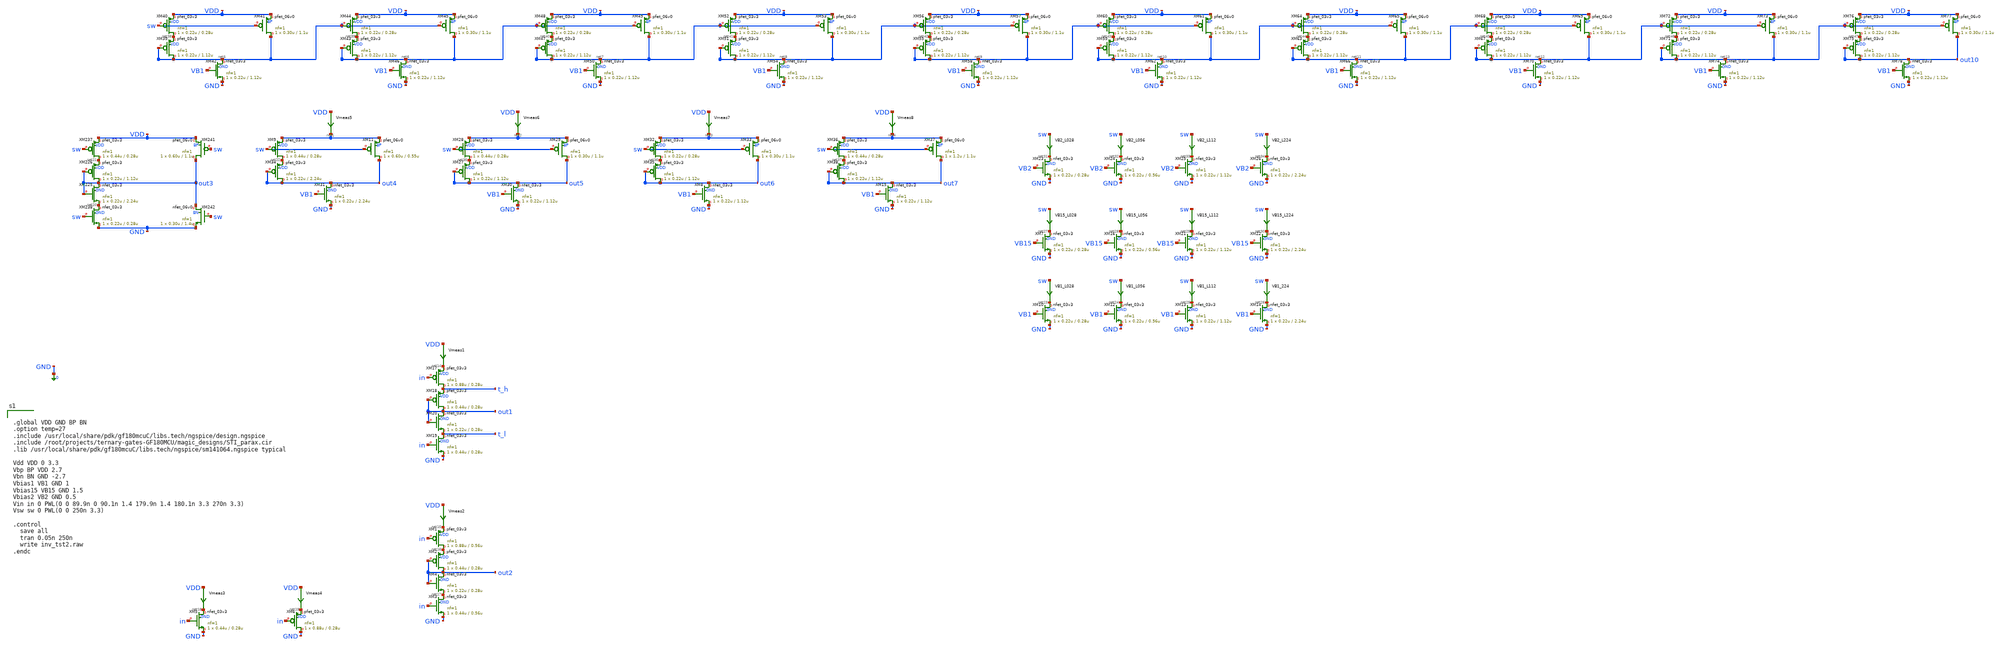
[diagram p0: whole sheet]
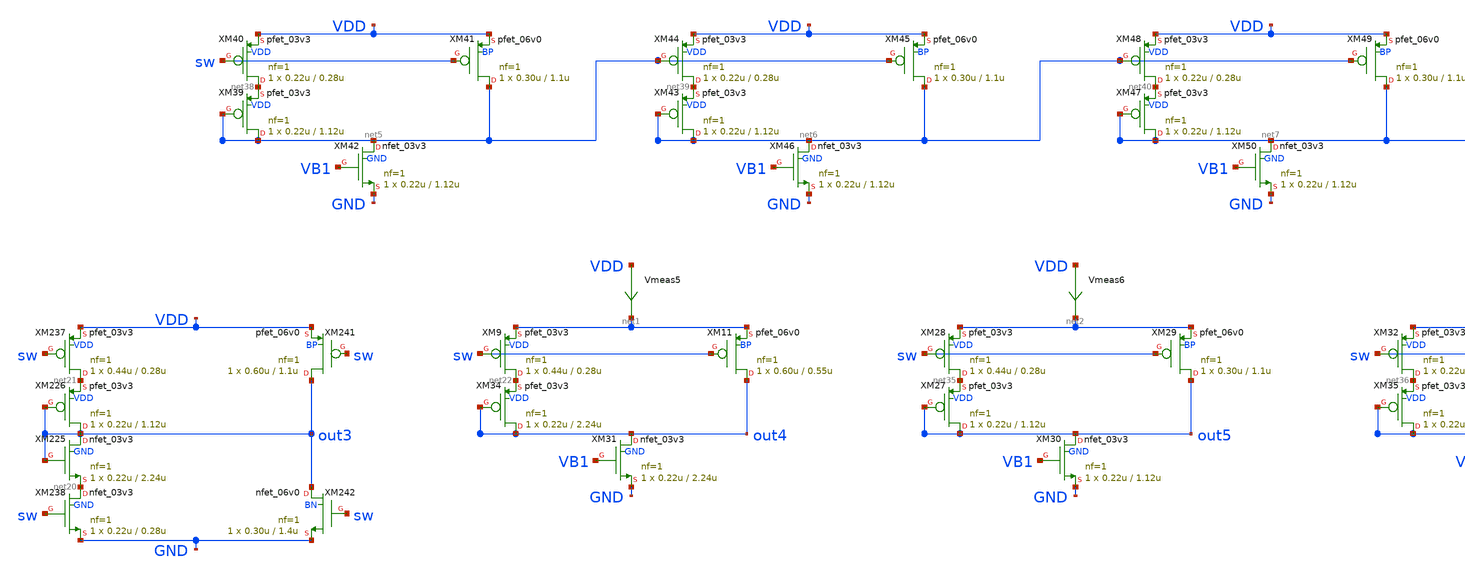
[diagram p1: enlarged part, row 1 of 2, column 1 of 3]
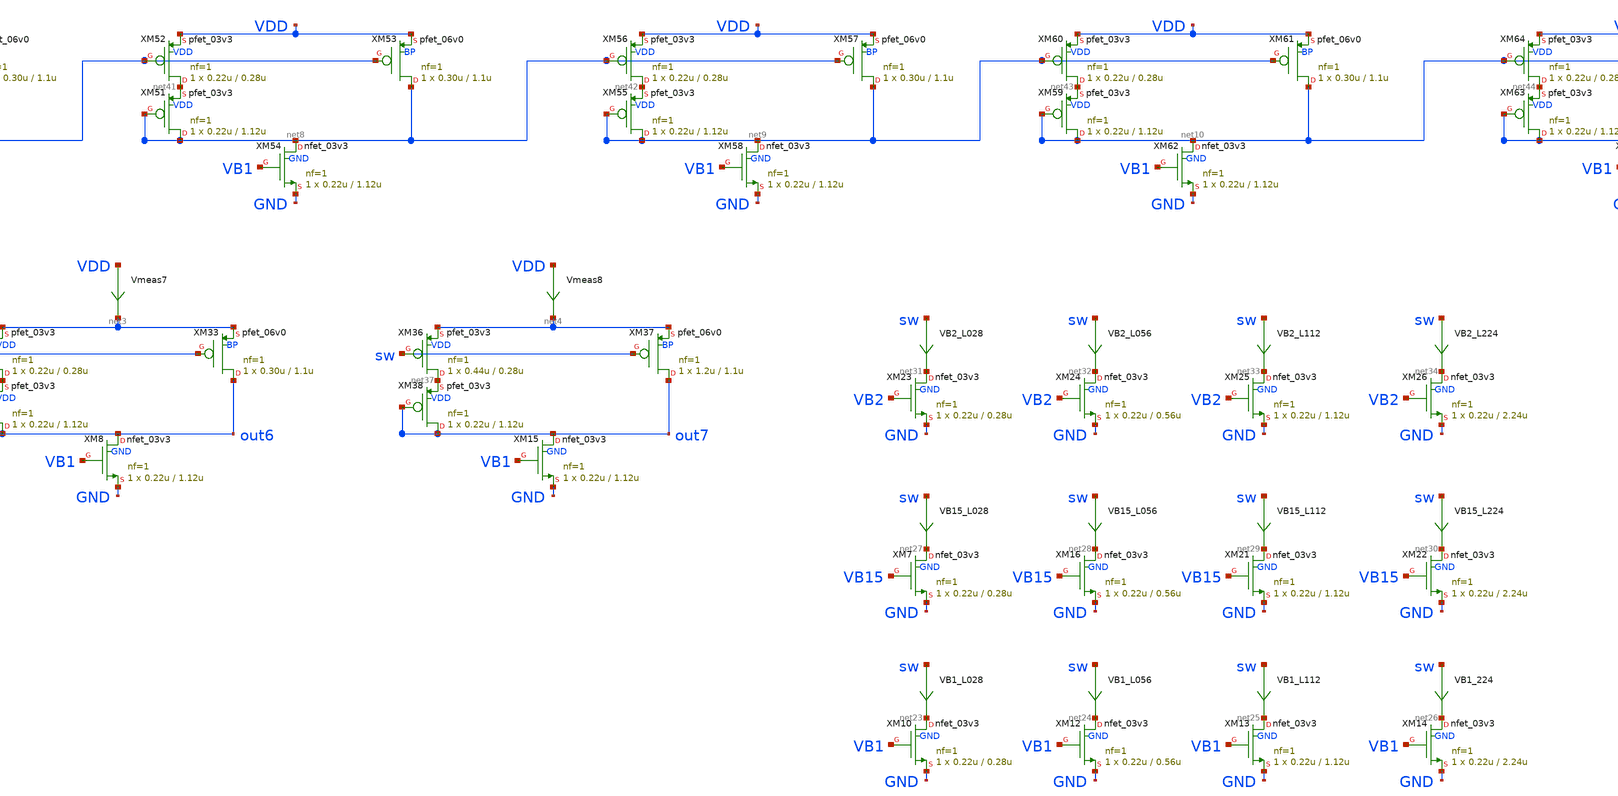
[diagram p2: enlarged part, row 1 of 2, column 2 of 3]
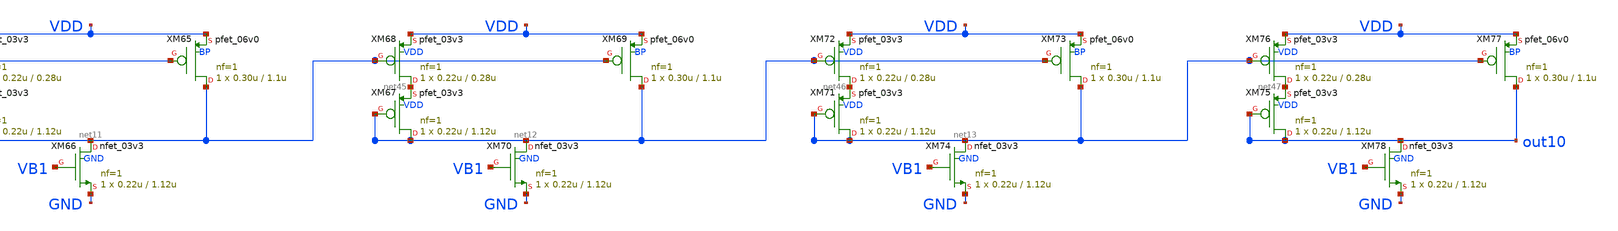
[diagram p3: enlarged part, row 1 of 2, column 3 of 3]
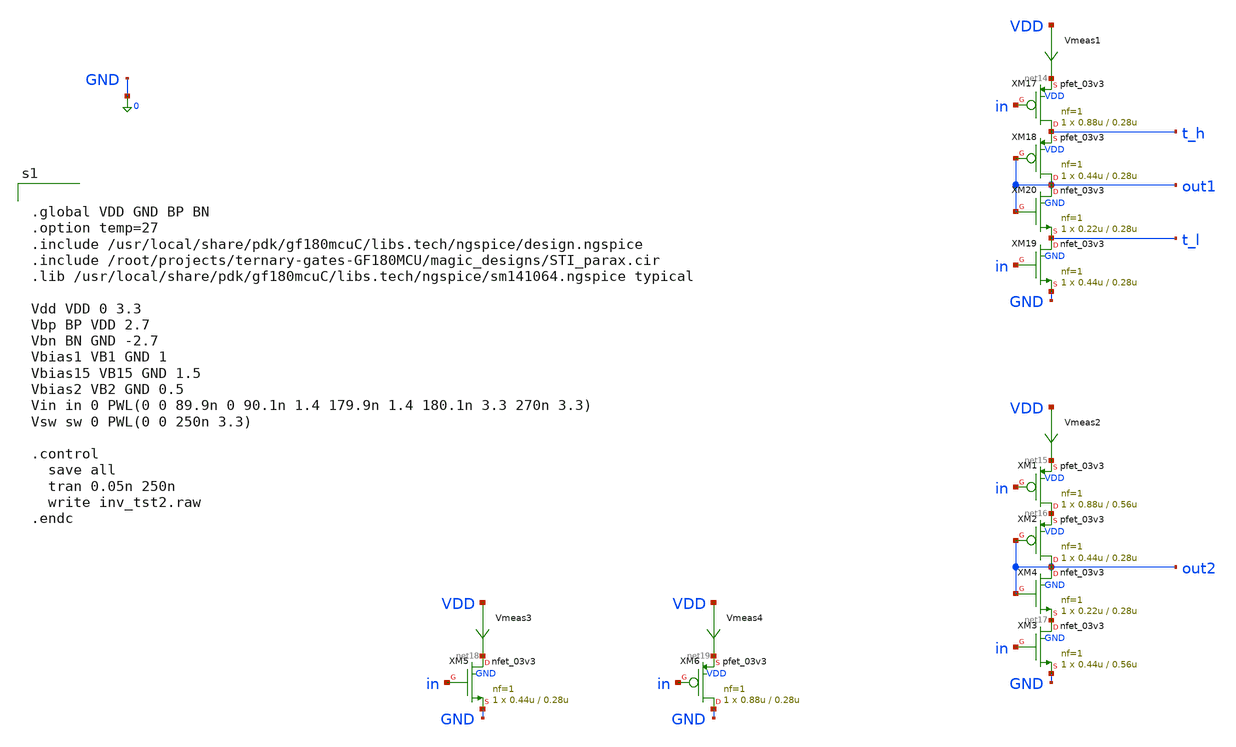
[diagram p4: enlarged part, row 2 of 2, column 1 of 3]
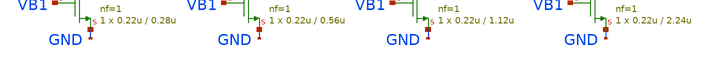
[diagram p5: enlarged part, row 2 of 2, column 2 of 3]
** sch_path: xschem_designs/inv_tst2.sch
**.subckt inv_tst2
Vmeas1 VDD net14 0
.save i(vmeas1)
XM17 t_h in net14 VDD pfet_03v3 L=0.28u W=0.88u nf=1 ad='int((nf+1)/2) * W/nf * 0.18u' as='int((nf+2)/2) * W/nf * 0.18u'
+ pd='2*int((nf+1)/2) * (W/nf + 0.18u)' ps='2*int((nf+2)/2) * (W/nf + 0.18u)' nrd='0.18u / W' nrs='0.18u / W'
+ sa=0 sb=0 sd=0 m=1 par=1
XM18 out1 out1 t_h VDD pfet_03v3 L=0.28u W=0.44u nf=1 ad='int((nf+1)/2) * W/nf * 0.18u' as='int((nf+2)/2) * W/nf * 0.18u'
+ pd='2*int((nf+1)/2) * (W/nf + 0.18u)' ps='2*int((nf+2)/2) * (W/nf + 0.18u)' nrd='0.18u / W' nrs='0.18u / W'
+ sa=0 sb=0 sd=0 m=1 par=1
XM19 t_l in GND GND nfet_03v3 L=0.28u W=0.44u nf=1 ad='int((nf+1)/2) * W/nf * 0.18u' as='int((nf+2)/2) * W/nf * 0.18u'
+ pd='2*int((nf+1)/2) * (W/nf + 0.18u)' ps='2*int((nf+2)/2) * (W/nf + 0.18u)' nrd='0.18u / W' nrs='0.18u / W'
+ sa=0 sb=0 sd=0 m=1 par=1
XM20 out1 out1 t_l GND nfet_03v3 L=0.28u W=0.22u nf=1 ad='int((nf+1)/2) * W/nf * 0.18u' as='int((nf+2)/2) * W/nf * 0.18u'
+ pd='2*int((nf+1)/2) * (W/nf + 0.18u)' ps='2*int((nf+2)/2) * (W/nf + 0.18u)' nrd='0.18u / W' nrs='0.18u / W'
+ sa=0 sb=0 sd=0 m=1 par=1
Vmeas2 VDD net15 0
.save i(vmeas2)
XM1 net16 in net15 VDD pfet_03v3 L=0.56u W=0.88u nf=1 ad='int((nf+1)/2) * W/nf * 0.18u' as='int((nf+2)/2) * W/nf * 0.18u'
+ pd='2*int((nf+1)/2) * (W/nf + 0.18u)' ps='2*int((nf+2)/2) * (W/nf + 0.18u)' nrd='0.18u / W' nrs='0.18u / W'
+ sa=0 sb=0 sd=0 m=1 par=1
XM2 out2 out2 net16 VDD pfet_03v3 L=0.28u W=0.44u nf=1 ad='int((nf+1)/2) * W/nf * 0.18u' as='int((nf+2)/2) * W/nf * 0.18u'
+ pd='2*int((nf+1)/2) * (W/nf + 0.18u)' ps='2*int((nf+2)/2) * (W/nf + 0.18u)' nrd='0.18u / W' nrs='0.18u / W'
+ sa=0 sb=0 sd=0 m=1 par=1
XM3 net17 in GND GND nfet_03v3 L=0.56u W=0.44u nf=1 ad='int((nf+1)/2) * W/nf * 0.18u' as='int((nf+2)/2) * W/nf * 0.18u'
+ pd='2*int((nf+1)/2) * (W/nf + 0.18u)' ps='2*int((nf+2)/2) * (W/nf + 0.18u)' nrd='0.18u / W' nrs='0.18u / W'
+ sa=0 sb=0 sd=0 m=1 par=1
XM4 out2 out2 net17 GND nfet_03v3 L=0.28u W=0.22u nf=1 ad='int((nf+1)/2) * W/nf * 0.18u' as='int((nf+2)/2) * W/nf * 0.18u'
+ pd='2*int((nf+1)/2) * (W/nf + 0.18u)' ps='2*int((nf+2)/2) * (W/nf + 0.18u)' nrd='0.18u / W' nrs='0.18u / W'
+ sa=0 sb=0 sd=0 m=1 par=1
XM5 net18 in GND GND nfet_03v3 L=0.28u W=0.44u nf=1 ad='int((nf+1)/2) * W/nf * 0.18u' as='int((nf+2)/2) * W/nf * 0.18u'
+ pd='2*int((nf+1)/2) * (W/nf + 0.18u)' ps='2*int((nf+2)/2) * (W/nf + 0.18u)' nrd='0.18u / W' nrs='0.18u / W'
+ sa=0 sb=0 sd=0 m=1 par=1
Vmeas3 VDD net18 0
.save i(vmeas3)
Vmeas4 VDD net19 0
.save i(vmeas4)
XM6 GND in net19 VDD pfet_03v3 L=0.28u W=0.88u nf=1 ad='int((nf+1)/2) * W/nf * 0.18u' as='int((nf+2)/2) * W/nf * 0.18u'
+ pd='2*int((nf+1)/2) * (W/nf + 0.18u)' ps='2*int((nf+2)/2) * (W/nf + 0.18u)' nrd='0.18u / W' nrs='0.18u / W'
+ sa=0 sb=0 sd=0 m=1 par=1
XM225 out3 out3 net20 GND nfet_03v3 L=2.24u W=0.22u nf=1 ad='int((nf+1)/2) * W/nf * 0.18u' as='int((nf+2)/2) * W/nf * 0.18u'
+ pd='2*int((nf+1)/2) * (W/nf + 0.18u)' ps='2*int((nf+2)/2) * (W/nf + 0.18u)' nrd='0.18u / W' nrs='0.18u / W'
+ sa=0 sb=0 sd=0 m=1 par=1
XM226 out3 out3 net21 VDD pfet_03v3 L=1.12u W=0.22u nf=1 ad='int((nf+1)/2) * W/nf * 0.18u' as='int((nf+2)/2) * W/nf * 0.18u'
+ pd='2*int((nf+1)/2) * (W/nf + 0.18u)' ps='2*int((nf+2)/2) * (W/nf + 0.18u)' nrd='0.18u / W' nrs='0.18u / W'
+ sa=0 sb=0 sd=0 m=1 par=1
XM237 net21 sw VDD VDD pfet_03v3 L=0.28u W=0.44u nf=1 ad='int((nf+1)/2) * W/nf * 0.18u' as='int((nf+2)/2) * W/nf * 0.18u'
+ pd='2*int((nf+1)/2) * (W/nf + 0.18u)' ps='2*int((nf+2)/2) * (W/nf + 0.18u)' nrd='0.18u / W' nrs='0.18u / W'
+ sa=0 sb=0 sd=0 m=1 par=1
XM238 net20 sw GND GND nfet_03v3 L=0.28u W=0.22u nf=1 ad='int((nf+1)/2) * W/nf * 0.18u' as='int((nf+2)/2) * W/nf * 0.18u'
+ pd='2*int((nf+1)/2) * (W/nf + 0.18u)' ps='2*int((nf+2)/2) * (W/nf + 0.18u)' nrd='0.18u / W' nrs='0.18u / W'
+ sa=0 sb=0 sd=0 m=1 par=1
XM241 out3 sw VDD BP pfet_06v0 L=1.1u W=0.60u nf=1 ad='int((nf+1)/2) * W/nf * 0.18u' as='int((nf+2)/2) * W/nf * 0.18u'
+ pd='2*int((nf+1)/2) * (W/nf + 0.18u)' ps='2*int((nf+2)/2) * (W/nf + 0.18u)' nrd='0.18u / W' nrs='0.18u / W'
+ sa=0 sb=0 sd=0 m=1 par=1
XM242 out3 sw GND BN nfet_06v0 L=1.4u W=0.30u nf=1 ad='int((nf+1)/2) * W/nf * 0.18u' as='int((nf+2)/2) * W/nf * 0.18u'
+ pd='2*int((nf+1)/2) * (W/nf + 0.18u)' ps='2*int((nf+2)/2) * (W/nf + 0.18u)' nrd='0.18u / W' nrs='0.18u / W'
+ sa=0 sb=0 sd=0 m=1 par=1
XM9 net22 sw net1 VDD pfet_03v3 L=0.28u W=0.44u nf=1 ad='int((nf+1)/2) * W/nf * 0.18u' as='int((nf+2)/2) * W/nf * 0.18u'
+ pd='2*int((nf+1)/2) * (W/nf + 0.18u)' ps='2*int((nf+2)/2) * (W/nf + 0.18u)' nrd='0.18u / W' nrs='0.18u / W'
+ sa=0 sb=0 sd=0 m=1 par=1
XM11 out4 sw net1 BP pfet_06v0 L=0.55u W=0.60u nf=1 ad='int((nf+1)/2) * W/nf * 0.18u' as='int((nf+2)/2) * W/nf * 0.18u'
+ pd='2*int((nf+1)/2) * (W/nf + 0.18u)' ps='2*int((nf+2)/2) * (W/nf + 0.18u)' nrd='0.18u / W' nrs='0.18u / W'
+ sa=0 sb=0 sd=0 m=1 par=1
Vmeas5 VDD net1 0
.save i(vmeas5)
XM10 net23 VB1 GND GND nfet_03v3 L=0.28u W=0.22u nf=1 ad='int((nf+1)/2) * W/nf * 0.18u' as='int((nf+2)/2) * W/nf * 0.18u'
+ pd='2*int((nf+1)/2) * (W/nf + 0.18u)' ps='2*int((nf+2)/2) * (W/nf + 0.18u)' nrd='0.18u / W' nrs='0.18u / W'
+ sa=0 sb=0 sd=0 m=1 par=1
VB1_L028 sw net23 0
.save i(vb1_l028)
XM12 net24 VB1 GND GND nfet_03v3 L=0.56u W=0.22u nf=1 ad='int((nf+1)/2) * W/nf * 0.18u' as='int((nf+2)/2) * W/nf * 0.18u'
+ pd='2*int((nf+1)/2) * (W/nf + 0.18u)' ps='2*int((nf+2)/2) * (W/nf + 0.18u)' nrd='0.18u / W' nrs='0.18u / W'
+ sa=0 sb=0 sd=0 m=1 par=1
XM13 net25 VB1 GND GND nfet_03v3 L=1.12u W=0.22u nf=1 ad='int((nf+1)/2) * W/nf * 0.18u' as='int((nf+2)/2) * W/nf * 0.18u'
+ pd='2*int((nf+1)/2) * (W/nf + 0.18u)' ps='2*int((nf+2)/2) * (W/nf + 0.18u)' nrd='0.18u / W' nrs='0.18u / W'
+ sa=0 sb=0 sd=0 m=1 par=1
XM14 net26 VB1 GND GND nfet_03v3 L=2.24u W=0.22u nf=1 ad='int((nf+1)/2) * W/nf * 0.18u' as='int((nf+2)/2) * W/nf * 0.18u'
+ pd='2*int((nf+1)/2) * (W/nf + 0.18u)' ps='2*int((nf+2)/2) * (W/nf + 0.18u)' nrd='0.18u / W' nrs='0.18u / W'
+ sa=0 sb=0 sd=0 m=1 par=1
VB1_L056 sw net24 0
.save i(vb1_l056)
VB1_L112 sw net25 0
.save i(vb1_l112)
VB1_224 sw net26 0
.save i(vb1_224)
XM7 net27 VB15 GND GND nfet_03v3 L=0.28u W=0.22u nf=1 ad='int((nf+1)/2) * W/nf * 0.18u' as='int((nf+2)/2) * W/nf * 0.18u'
+ pd='2*int((nf+1)/2) * (W/nf + 0.18u)' ps='2*int((nf+2)/2) * (W/nf + 0.18u)' nrd='0.18u / W' nrs='0.18u / W'
+ sa=0 sb=0 sd=0 m=1 par=1
VB15_L028 sw net27 0
.save i(vb15_l028)
XM16 net28 VB15 GND GND nfet_03v3 L=0.56u W=0.22u nf=1 ad='int((nf+1)/2) * W/nf * 0.18u' as='int((nf+2)/2) * W/nf * 0.18u'
+ pd='2*int((nf+1)/2) * (W/nf + 0.18u)' ps='2*int((nf+2)/2) * (W/nf + 0.18u)' nrd='0.18u / W' nrs='0.18u / W'
+ sa=0 sb=0 sd=0 m=1 par=1
XM21 net29 VB15 GND GND nfet_03v3 L=1.12u W=0.22u nf=1 ad='int((nf+1)/2) * W/nf * 0.18u' as='int((nf+2)/2) * W/nf * 0.18u'
+ pd='2*int((nf+1)/2) * (W/nf + 0.18u)' ps='2*int((nf+2)/2) * (W/nf + 0.18u)' nrd='0.18u / W' nrs='0.18u / W'
+ sa=0 sb=0 sd=0 m=1 par=1
XM22 net30 VB15 GND GND nfet_03v3 L=2.24u W=0.22u nf=1 ad='int((nf+1)/2) * W/nf * 0.18u' as='int((nf+2)/2) * W/nf * 0.18u'
+ pd='2*int((nf+1)/2) * (W/nf + 0.18u)' ps='2*int((nf+2)/2) * (W/nf + 0.18u)' nrd='0.18u / W' nrs='0.18u / W'
+ sa=0 sb=0 sd=0 m=1 par=1
VB15_L056 sw net28 0
.save i(vb15_l056)
VB15_L112 sw net29 0
.save i(vb15_l112)
VB15_L224 sw net30 0
.save i(vb15_l224)
XM23 net31 VB2 GND GND nfet_03v3 L=0.28u W=0.22u nf=1 ad='int((nf+1)/2) * W/nf * 0.18u' as='int((nf+2)/2) * W/nf * 0.18u'
+ pd='2*int((nf+1)/2) * (W/nf + 0.18u)' ps='2*int((nf+2)/2) * (W/nf + 0.18u)' nrd='0.18u / W' nrs='0.18u / W'
+ sa=0 sb=0 sd=0 m=1 par=1
VB2_L028 sw net31 0
.save i(vb2_l028)
XM24 net32 VB2 GND GND nfet_03v3 L=0.56u W=0.22u nf=1 ad='int((nf+1)/2) * W/nf * 0.18u' as='int((nf+2)/2) * W/nf * 0.18u'
+ pd='2*int((nf+1)/2) * (W/nf + 0.18u)' ps='2*int((nf+2)/2) * (W/nf + 0.18u)' nrd='0.18u / W' nrs='0.18u / W'
+ sa=0 sb=0 sd=0 m=1 par=1
XM25 net33 VB2 GND GND nfet_03v3 L=1.12u W=0.22u nf=1 ad='int((nf+1)/2) * W/nf * 0.18u' as='int((nf+2)/2) * W/nf * 0.18u'
+ pd='2*int((nf+1)/2) * (W/nf + 0.18u)' ps='2*int((nf+2)/2) * (W/nf + 0.18u)' nrd='0.18u / W' nrs='0.18u / W'
+ sa=0 sb=0 sd=0 m=1 par=1
XM26 net34 VB2 GND GND nfet_03v3 L=2.24u W=0.22u nf=1 ad='int((nf+1)/2) * W/nf * 0.18u' as='int((nf+2)/2) * W/nf * 0.18u'
+ pd='2*int((nf+1)/2) * (W/nf + 0.18u)' ps='2*int((nf+2)/2) * (W/nf + 0.18u)' nrd='0.18u / W' nrs='0.18u / W'
+ sa=0 sb=0 sd=0 m=1 par=1
VB2_L056 sw net32 0
.save i(vb2_l056)
VB2_L112 sw net33 0
.save i(vb2_l112)
VB2_L224 sw net34 0
.save i(vb2_l224)
XM28 net35 sw net2 VDD pfet_03v3 L=0.28u W=0.44u nf=1 ad='int((nf+1)/2) * W/nf * 0.18u' as='int((nf+2)/2) * W/nf * 0.18u'
+ pd='2*int((nf+1)/2) * (W/nf + 0.18u)' ps='2*int((nf+2)/2) * (W/nf + 0.18u)' nrd='0.18u / W' nrs='0.18u / W'
+ sa=0 sb=0 sd=0 m=1 par=1
XM29 out5 sw net2 BP pfet_06v0 L=1.1u W=0.30u nf=1 ad='int((nf+1)/2) * W/nf * 0.18u' as='int((nf+2)/2) * W/nf * 0.18u'
+ pd='2*int((nf+1)/2) * (W/nf + 0.18u)' ps='2*int((nf+2)/2) * (W/nf + 0.18u)' nrd='0.18u / W' nrs='0.18u / W'
+ sa=0 sb=0 sd=0 m=1 par=1
Vmeas6 VDD net2 0
.save i(vmeas6)
XM32 net36 sw net3 VDD pfet_03v3 L=0.28u W=0.22u nf=1 ad='int((nf+1)/2) * W/nf * 0.18u' as='int((nf+2)/2) * W/nf * 0.18u'
+ pd='2*int((nf+1)/2) * (W/nf + 0.18u)' ps='2*int((nf+2)/2) * (W/nf + 0.18u)' nrd='0.18u / W' nrs='0.18u / W'
+ sa=0 sb=0 sd=0 m=1 par=1
Vmeas7 VDD net3 0
.save i(vmeas7)
XM36 net37 sw net4 VDD pfet_03v3 L=0.28u W=0.44u nf=1 ad='int((nf+1)/2) * W/nf * 0.18u' as='int((nf+2)/2) * W/nf * 0.18u'
+ pd='2*int((nf+1)/2) * (W/nf + 0.18u)' ps='2*int((nf+2)/2) * (W/nf + 0.18u)' nrd='0.18u / W' nrs='0.18u / W'
+ sa=0 sb=0 sd=0 m=1 par=1
XM37 out7 sw net4 BP pfet_06v0 L=1.1u W=1.2u nf=1 ad='int((nf+1)/2) * W/nf * 0.18u' as='int((nf+2)/2) * W/nf * 0.18u'
+ pd='2*int((nf+1)/2) * (W/nf + 0.18u)' ps='2*int((nf+2)/2) * (W/nf + 0.18u)' nrd='0.18u / W' nrs='0.18u / W'
+ sa=0 sb=0 sd=0 m=1 par=1
Vmeas8 VDD net4 0
.save i(vmeas8)
XM8 out6 VB1 GND GND nfet_03v3 L=1.12u W=0.22u nf=1 ad='int((nf+1)/2) * W/nf * 0.18u' as='int((nf+2)/2) * W/nf * 0.18u'
+ pd='2*int((nf+1)/2) * (W/nf + 0.18u)' ps='2*int((nf+2)/2) * (W/nf + 0.18u)' nrd='0.18u / W' nrs='0.18u / W'
+ sa=0 sb=0 sd=0 m=1 par=1
XM15 out7 VB1 GND GND nfet_03v3 L=1.12u W=0.22u nf=1 ad='int((nf+1)/2) * W/nf * 0.18u' as='int((nf+2)/2) * W/nf * 0.18u'
+ pd='2*int((nf+1)/2) * (W/nf + 0.18u)' ps='2*int((nf+2)/2) * (W/nf + 0.18u)' nrd='0.18u / W' nrs='0.18u / W'
+ sa=0 sb=0 sd=0 m=1 par=1
XM31 out4 VB1 GND GND nfet_03v3 L=2.24u W=0.22u nf=1 ad='int((nf+1)/2) * W/nf * 0.18u' as='int((nf+2)/2) * W/nf * 0.18u'
+ pd='2*int((nf+1)/2) * (W/nf + 0.18u)' ps='2*int((nf+2)/2) * (W/nf + 0.18u)' nrd='0.18u / W' nrs='0.18u / W'
+ sa=0 sb=0 sd=0 m=1 par=1
XM34 out4 out4 net22 VDD pfet_03v3 L=2.24u W=0.22u nf=1 ad='int((nf+1)/2) * W/nf * 0.18u' as='int((nf+2)/2) * W/nf * 0.18u'
+ pd='2*int((nf+1)/2) * (W/nf + 0.18u)' ps='2*int((nf+2)/2) * (W/nf + 0.18u)' nrd='0.18u / W' nrs='0.18u / W'
+ sa=0 sb=0 sd=0 m=1 par=1
XM35 out6 out6 net36 VDD pfet_03v3 L=1.12u W=0.22u nf=1 ad='int((nf+1)/2) * W/nf * 0.18u' as='int((nf+2)/2) * W/nf * 0.18u'
+ pd='2*int((nf+1)/2) * (W/nf + 0.18u)' ps='2*int((nf+2)/2) * (W/nf + 0.18u)' nrd='0.18u / W' nrs='0.18u / W'
+ sa=0 sb=0 sd=0 m=1 par=1
XM38 out7 out7 net37 VDD pfet_03v3 L=1.12u W=0.22u nf=1 ad='int((nf+1)/2) * W/nf * 0.18u' as='int((nf+2)/2) * W/nf * 0.18u'
+ pd='2*int((nf+1)/2) * (W/nf + 0.18u)' ps='2*int((nf+2)/2) * (W/nf + 0.18u)' nrd='0.18u / W' nrs='0.18u / W'
+ sa=0 sb=0 sd=0 m=1 par=1
XM39 net5 net5 net38 VDD pfet_03v3 L=1.12u W=0.22u nf=1 ad='int((nf+1)/2) * W/nf * 0.18u' as='int((nf+2)/2) * W/nf * 0.18u'
+ pd='2*int((nf+1)/2) * (W/nf + 0.18u)' ps='2*int((nf+2)/2) * (W/nf + 0.18u)' nrd='0.18u / W' nrs='0.18u / W'
+ sa=0 sb=0 sd=0 m=1 par=1
XM42 net5 VB1 GND GND nfet_03v3 L=1.12u W=0.22u nf=1 ad='int((nf+1)/2) * W/nf * 0.18u' as='int((nf+2)/2) * W/nf * 0.18u'
+ pd='2*int((nf+1)/2) * (W/nf + 0.18u)' ps='2*int((nf+2)/2) * (W/nf + 0.18u)' nrd='0.18u / W' nrs='0.18u / W'
+ sa=0 sb=0 sd=0 m=1 par=1
XM43 net6 net6 net39 VDD pfet_03v3 L=1.12u W=0.22u nf=1 ad='int((nf+1)/2) * W/nf * 0.18u' as='int((nf+2)/2) * W/nf * 0.18u'
+ pd='2*int((nf+1)/2) * (W/nf + 0.18u)' ps='2*int((nf+2)/2) * (W/nf + 0.18u)' nrd='0.18u / W' nrs='0.18u / W'
+ sa=0 sb=0 sd=0 m=1 par=1
XM46 net6 VB1 GND GND nfet_03v3 L=1.12u W=0.22u nf=1 ad='int((nf+1)/2) * W/nf * 0.18u' as='int((nf+2)/2) * W/nf * 0.18u'
+ pd='2*int((nf+1)/2) * (W/nf + 0.18u)' ps='2*int((nf+2)/2) * (W/nf + 0.18u)' nrd='0.18u / W' nrs='0.18u / W'
+ sa=0 sb=0 sd=0 m=1 par=1
XM47 net7 net7 net40 VDD pfet_03v3 L=1.12u W=0.22u nf=1 ad='int((nf+1)/2) * W/nf * 0.18u' as='int((nf+2)/2) * W/nf * 0.18u'
+ pd='2*int((nf+1)/2) * (W/nf + 0.18u)' ps='2*int((nf+2)/2) * (W/nf + 0.18u)' nrd='0.18u / W' nrs='0.18u / W'
+ sa=0 sb=0 sd=0 m=1 par=1
XM50 net7 VB1 GND GND nfet_03v3 L=1.12u W=0.22u nf=1 ad='int((nf+1)/2) * W/nf * 0.18u' as='int((nf+2)/2) * W/nf * 0.18u'
+ pd='2*int((nf+1)/2) * (W/nf + 0.18u)' ps='2*int((nf+2)/2) * (W/nf + 0.18u)' nrd='0.18u / W' nrs='0.18u / W'
+ sa=0 sb=0 sd=0 m=1 par=1
XM51 net8 net8 net41 VDD pfet_03v3 L=1.12u W=0.22u nf=1 ad='int((nf+1)/2) * W/nf * 0.18u' as='int((nf+2)/2) * W/nf * 0.18u'
+ pd='2*int((nf+1)/2) * (W/nf + 0.18u)' ps='2*int((nf+2)/2) * (W/nf + 0.18u)' nrd='0.18u / W' nrs='0.18u / W'
+ sa=0 sb=0 sd=0 m=1 par=1
XM54 net8 VB1 GND GND nfet_03v3 L=1.12u W=0.22u nf=1 ad='int((nf+1)/2) * W/nf * 0.18u' as='int((nf+2)/2) * W/nf * 0.18u'
+ pd='2*int((nf+1)/2) * (W/nf + 0.18u)' ps='2*int((nf+2)/2) * (W/nf + 0.18u)' nrd='0.18u / W' nrs='0.18u / W'
+ sa=0 sb=0 sd=0 m=1 par=1
XM55 net9 net9 net42 VDD pfet_03v3 L=1.12u W=0.22u nf=1 ad='int((nf+1)/2) * W/nf * 0.18u' as='int((nf+2)/2) * W/nf * 0.18u'
+ pd='2*int((nf+1)/2) * (W/nf + 0.18u)' ps='2*int((nf+2)/2) * (W/nf + 0.18u)' nrd='0.18u / W' nrs='0.18u / W'
+ sa=0 sb=0 sd=0 m=1 par=1
XM58 net9 VB1 GND GND nfet_03v3 L=1.12u W=0.22u nf=1 ad='int((nf+1)/2) * W/nf * 0.18u' as='int((nf+2)/2) * W/nf * 0.18u'
+ pd='2*int((nf+1)/2) * (W/nf + 0.18u)' ps='2*int((nf+2)/2) * (W/nf + 0.18u)' nrd='0.18u / W' nrs='0.18u / W'
+ sa=0 sb=0 sd=0 m=1 par=1
XM59 net10 net10 net43 VDD pfet_03v3 L=1.12u W=0.22u nf=1 ad='int((nf+1)/2) * W/nf * 0.18u' as='int((nf+2)/2) * W/nf * 0.18u'
+ pd='2*int((nf+1)/2) * (W/nf + 0.18u)' ps='2*int((nf+2)/2) * (W/nf + 0.18u)' nrd='0.18u / W' nrs='0.18u / W'
+ sa=0 sb=0 sd=0 m=1 par=1
XM62 net10 VB1 GND GND nfet_03v3 L=1.12u W=0.22u nf=1 ad='int((nf+1)/2) * W/nf * 0.18u' as='int((nf+2)/2) * W/nf * 0.18u'
+ pd='2*int((nf+1)/2) * (W/nf + 0.18u)' ps='2*int((nf+2)/2) * (W/nf + 0.18u)' nrd='0.18u / W' nrs='0.18u / W'
+ sa=0 sb=0 sd=0 m=1 par=1
XM63 net11 net11 net44 VDD pfet_03v3 L=1.12u W=0.22u nf=1 ad='int((nf+1)/2) * W/nf * 0.18u' as='int((nf+2)/2) * W/nf * 0.18u'
+ pd='2*int((nf+1)/2) * (W/nf + 0.18u)' ps='2*int((nf+2)/2) * (W/nf + 0.18u)' nrd='0.18u / W' nrs='0.18u / W'
+ sa=0 sb=0 sd=0 m=1 par=1
XM66 net11 VB1 GND GND nfet_03v3 L=1.12u W=0.22u nf=1 ad='int((nf+1)/2) * W/nf * 0.18u' as='int((nf+2)/2) * W/nf * 0.18u'
+ pd='2*int((nf+1)/2) * (W/nf + 0.18u)' ps='2*int((nf+2)/2) * (W/nf + 0.18u)' nrd='0.18u / W' nrs='0.18u / W'
+ sa=0 sb=0 sd=0 m=1 par=1
XM67 net12 net12 net45 VDD pfet_03v3 L=1.12u W=0.22u nf=1 ad='int((nf+1)/2) * W/nf * 0.18u' as='int((nf+2)/2) * W/nf * 0.18u'
+ pd='2*int((nf+1)/2) * (W/nf + 0.18u)' ps='2*int((nf+2)/2) * (W/nf + 0.18u)' nrd='0.18u / W' nrs='0.18u / W'
+ sa=0 sb=0 sd=0 m=1 par=1
XM70 net12 VB1 GND GND nfet_03v3 L=1.12u W=0.22u nf=1 ad='int((nf+1)/2) * W/nf * 0.18u' as='int((nf+2)/2) * W/nf * 0.18u'
+ pd='2*int((nf+1)/2) * (W/nf + 0.18u)' ps='2*int((nf+2)/2) * (W/nf + 0.18u)' nrd='0.18u / W' nrs='0.18u / W'
+ sa=0 sb=0 sd=0 m=1 par=1
XM71 net13 net13 net46 VDD pfet_03v3 L=1.12u W=0.22u nf=1 ad='int((nf+1)/2) * W/nf * 0.18u' as='int((nf+2)/2) * W/nf * 0.18u'
+ pd='2*int((nf+1)/2) * (W/nf + 0.18u)' ps='2*int((nf+2)/2) * (W/nf + 0.18u)' nrd='0.18u / W' nrs='0.18u / W'
+ sa=0 sb=0 sd=0 m=1 par=1
XM74 net13 VB1 GND GND nfet_03v3 L=1.12u W=0.22u nf=1 ad='int((nf+1)/2) * W/nf * 0.18u' as='int((nf+2)/2) * W/nf * 0.18u'
+ pd='2*int((nf+1)/2) * (W/nf + 0.18u)' ps='2*int((nf+2)/2) * (W/nf + 0.18u)' nrd='0.18u / W' nrs='0.18u / W'
+ sa=0 sb=0 sd=0 m=1 par=1
XM75 out10 out10 net47 VDD pfet_03v3 L=1.12u W=0.22u nf=1 ad='int((nf+1)/2) * W/nf * 0.18u' as='int((nf+2)/2) * W/nf * 0.18u'
+ pd='2*int((nf+1)/2) * (W/nf + 0.18u)' ps='2*int((nf+2)/2) * (W/nf + 0.18u)' nrd='0.18u / W' nrs='0.18u / W'
+ sa=0 sb=0 sd=0 m=1 par=1
XM78 out10 VB1 GND GND nfet_03v3 L=1.12u W=0.22u nf=1 ad='int((nf+1)/2) * W/nf * 0.18u' as='int((nf+2)/2) * W/nf * 0.18u'
+ pd='2*int((nf+1)/2) * (W/nf + 0.18u)' ps='2*int((nf+2)/2) * (W/nf + 0.18u)' nrd='0.18u / W' nrs='0.18u / W'
+ sa=0 sb=0 sd=0 m=1 par=1
XM27 out5 out5 net35 VDD pfet_03v3 L=1.12u W=0.22u nf=1 ad='int((nf+1)/2) * W/nf * 0.18u' as='int((nf+2)/2) * W/nf * 0.18u'
+ pd='2*int((nf+1)/2) * (W/nf + 0.18u)' ps='2*int((nf+2)/2) * (W/nf + 0.18u)' nrd='0.18u / W' nrs='0.18u / W'
+ sa=0 sb=0 sd=0 m=1 par=1
XM30 out5 VB1 GND GND nfet_03v3 L=1.12u W=0.22u nf=1 ad='int((nf+1)/2) * W/nf * 0.18u' as='int((nf+2)/2) * W/nf * 0.18u'
+ pd='2*int((nf+1)/2) * (W/nf + 0.18u)' ps='2*int((nf+2)/2) * (W/nf + 0.18u)' nrd='0.18u / W' nrs='0.18u / W'
+ sa=0 sb=0 sd=0 m=1 par=1
XM41 net5 sw VDD BP pfet_06v0 L=1.1u W=0.30u nf=1 ad='int((nf+1)/2) * W/nf * 0.18u' as='int((nf+2)/2) * W/nf * 0.18u'
+ pd='2*int((nf+1)/2) * (W/nf + 0.18u)' ps='2*int((nf+2)/2) * (W/nf + 0.18u)' nrd='0.18u / W' nrs='0.18u / W'
+ sa=0 sb=0 sd=0 m=1 par=1
XM45 net6 net5 VDD BP pfet_06v0 L=1.1u W=0.30u nf=1 ad='int((nf+1)/2) * W/nf * 0.18u' as='int((nf+2)/2) * W/nf * 0.18u'
+ pd='2*int((nf+1)/2) * (W/nf + 0.18u)' ps='2*int((nf+2)/2) * (W/nf + 0.18u)' nrd='0.18u / W' nrs='0.18u / W'
+ sa=0 sb=0 sd=0 m=1 par=1
XM49 net7 net6 VDD BP pfet_06v0 L=1.1u W=0.30u nf=1 ad='int((nf+1)/2) * W/nf * 0.18u' as='int((nf+2)/2) * W/nf * 0.18u'
+ pd='2*int((nf+1)/2) * (W/nf + 0.18u)' ps='2*int((nf+2)/2) * (W/nf + 0.18u)' nrd='0.18u / W' nrs='0.18u / W'
+ sa=0 sb=0 sd=0 m=1 par=1
XM53 net8 net7 VDD BP pfet_06v0 L=1.1u W=0.30u nf=1 ad='int((nf+1)/2) * W/nf * 0.18u' as='int((nf+2)/2) * W/nf * 0.18u'
+ pd='2*int((nf+1)/2) * (W/nf + 0.18u)' ps='2*int((nf+2)/2) * (W/nf + 0.18u)' nrd='0.18u / W' nrs='0.18u / W'
+ sa=0 sb=0 sd=0 m=1 par=1
XM57 net9 net8 VDD BP pfet_06v0 L=1.1u W=0.30u nf=1 ad='int((nf+1)/2) * W/nf * 0.18u' as='int((nf+2)/2) * W/nf * 0.18u'
+ pd='2*int((nf+1)/2) * (W/nf + 0.18u)' ps='2*int((nf+2)/2) * (W/nf + 0.18u)' nrd='0.18u / W' nrs='0.18u / W'
+ sa=0 sb=0 sd=0 m=1 par=1
XM61 net10 net9 VDD BP pfet_06v0 L=1.1u W=0.30u nf=1 ad='int((nf+1)/2) * W/nf * 0.18u' as='int((nf+2)/2) * W/nf * 0.18u'
+ pd='2*int((nf+1)/2) * (W/nf + 0.18u)' ps='2*int((nf+2)/2) * (W/nf + 0.18u)' nrd='0.18u / W' nrs='0.18u / W'
+ sa=0 sb=0 sd=0 m=1 par=1
XM65 net11 net10 VDD BP pfet_06v0 L=1.1u W=0.30u nf=1 ad='int((nf+1)/2) * W/nf * 0.18u' as='int((nf+2)/2) * W/nf * 0.18u'
+ pd='2*int((nf+1)/2) * (W/nf + 0.18u)' ps='2*int((nf+2)/2) * (W/nf + 0.18u)' nrd='0.18u / W' nrs='0.18u / W'
+ sa=0 sb=0 sd=0 m=1 par=1
XM69 net12 net11 VDD BP pfet_06v0 L=1.1u W=0.30u nf=1 ad='int((nf+1)/2) * W/nf * 0.18u' as='int((nf+2)/2) * W/nf * 0.18u'
+ pd='2*int((nf+1)/2) * (W/nf + 0.18u)' ps='2*int((nf+2)/2) * (W/nf + 0.18u)' nrd='0.18u / W' nrs='0.18u / W'
+ sa=0 sb=0 sd=0 m=1 par=1
XM73 net13 net12 VDD BP pfet_06v0 L=1.1u W=0.30u nf=1 ad='int((nf+1)/2) * W/nf * 0.18u' as='int((nf+2)/2) * W/nf * 0.18u'
+ pd='2*int((nf+1)/2) * (W/nf + 0.18u)' ps='2*int((nf+2)/2) * (W/nf + 0.18u)' nrd='0.18u / W' nrs='0.18u / W'
+ sa=0 sb=0 sd=0 m=1 par=1
XM77 out10 net13 VDD BP pfet_06v0 L=1.1u W=0.30u nf=1 ad='int((nf+1)/2) * W/nf * 0.18u' as='int((nf+2)/2) * W/nf * 0.18u'
+ pd='2*int((nf+1)/2) * (W/nf + 0.18u)' ps='2*int((nf+2)/2) * (W/nf + 0.18u)' nrd='0.18u / W' nrs='0.18u / W'
+ sa=0 sb=0 sd=0 m=1 par=1
XM33 out6 sw net3 BP pfet_06v0 L=1.1u W=0.30u nf=1 ad='int((nf+1)/2) * W/nf * 0.18u' as='int((nf+2)/2) * W/nf * 0.18u'
+ pd='2*int((nf+1)/2) * (W/nf + 0.18u)' ps='2*int((nf+2)/2) * (W/nf + 0.18u)' nrd='0.18u / W' nrs='0.18u / W'
+ sa=0 sb=0 sd=0 m=1 par=1
XM40 net38 sw VDD VDD pfet_03v3 L=0.28u W=0.22u nf=1 ad='int((nf+1)/2) * W/nf * 0.18u' as='int((nf+2)/2) * W/nf * 0.18u'
+ pd='2*int((nf+1)/2) * (W/nf + 0.18u)' ps='2*int((nf+2)/2) * (W/nf + 0.18u)' nrd='0.18u / W' nrs='0.18u / W'
+ sa=0 sb=0 sd=0 m=1 par=1
XM44 net39 net5 VDD VDD pfet_03v3 L=0.28u W=0.22u nf=1 ad='int((nf+1)/2) * W/nf * 0.18u' as='int((nf+2)/2) * W/nf * 0.18u'
+ pd='2*int((nf+1)/2) * (W/nf + 0.18u)' ps='2*int((nf+2)/2) * (W/nf + 0.18u)' nrd='0.18u / W' nrs='0.18u / W'
+ sa=0 sb=0 sd=0 m=1 par=1
XM48 net40 net6 VDD VDD pfet_03v3 L=0.28u W=0.22u nf=1 ad='int((nf+1)/2) * W/nf * 0.18u' as='int((nf+2)/2) * W/nf * 0.18u'
+ pd='2*int((nf+1)/2) * (W/nf + 0.18u)' ps='2*int((nf+2)/2) * (W/nf + 0.18u)' nrd='0.18u / W' nrs='0.18u / W'
+ sa=0 sb=0 sd=0 m=1 par=1
XM52 net41 net7 VDD VDD pfet_03v3 L=0.28u W=0.22u nf=1 ad='int((nf+1)/2) * W/nf * 0.18u' as='int((nf+2)/2) * W/nf * 0.18u'
+ pd='2*int((nf+1)/2) * (W/nf + 0.18u)' ps='2*int((nf+2)/2) * (W/nf + 0.18u)' nrd='0.18u / W' nrs='0.18u / W'
+ sa=0 sb=0 sd=0 m=1 par=1
XM56 net42 net8 VDD VDD pfet_03v3 L=0.28u W=0.22u nf=1 ad='int((nf+1)/2) * W/nf * 0.18u' as='int((nf+2)/2) * W/nf * 0.18u'
+ pd='2*int((nf+1)/2) * (W/nf + 0.18u)' ps='2*int((nf+2)/2) * (W/nf + 0.18u)' nrd='0.18u / W' nrs='0.18u / W'
+ sa=0 sb=0 sd=0 m=1 par=1
XM60 net43 net9 VDD VDD pfet_03v3 L=0.28u W=0.22u nf=1 ad='int((nf+1)/2) * W/nf * 0.18u' as='int((nf+2)/2) * W/nf * 0.18u'
+ pd='2*int((nf+1)/2) * (W/nf + 0.18u)' ps='2*int((nf+2)/2) * (W/nf + 0.18u)' nrd='0.18u / W' nrs='0.18u / W'
+ sa=0 sb=0 sd=0 m=1 par=1
XM64 net44 net10 VDD VDD pfet_03v3 L=0.28u W=0.22u nf=1 ad='int((nf+1)/2) * W/nf * 0.18u' as='int((nf+2)/2) * W/nf * 0.18u'
+ pd='2*int((nf+1)/2) * (W/nf + 0.18u)' ps='2*int((nf+2)/2) * (W/nf + 0.18u)' nrd='0.18u / W' nrs='0.18u / W'
+ sa=0 sb=0 sd=0 m=1 par=1
XM68 net45 net11 VDD VDD pfet_03v3 L=0.28u W=0.22u nf=1 ad='int((nf+1)/2) * W/nf * 0.18u' as='int((nf+2)/2) * W/nf * 0.18u'
+ pd='2*int((nf+1)/2) * (W/nf + 0.18u)' ps='2*int((nf+2)/2) * (W/nf + 0.18u)' nrd='0.18u / W' nrs='0.18u / W'
+ sa=0 sb=0 sd=0 m=1 par=1
XM72 net46 net12 VDD VDD pfet_03v3 L=0.28u W=0.22u nf=1 ad='int((nf+1)/2) * W/nf * 0.18u' as='int((nf+2)/2) * W/nf * 0.18u'
+ pd='2*int((nf+1)/2) * (W/nf + 0.18u)' ps='2*int((nf+2)/2) * (W/nf + 0.18u)' nrd='0.18u / W' nrs='0.18u / W'
+ sa=0 sb=0 sd=0 m=1 par=1
XM76 net47 net13 VDD VDD pfet_03v3 L=0.28u W=0.22u nf=1 ad='int((nf+1)/2) * W/nf * 0.18u' as='int((nf+2)/2) * W/nf * 0.18u'
+ pd='2*int((nf+1)/2) * (W/nf + 0.18u)' ps='2*int((nf+2)/2) * (W/nf + 0.18u)' nrd='0.18u / W' nrs='0.18u / W'
+ sa=0 sb=0 sd=0 m=1 par=1
**** begin user architecture code


.global VDD GND BP BN
.option temp=27
.include /usr/local/share/pdk/gf180mcuC/libs.tech/ngspice/design.ngspice
.include /root/projects/ternary-gates-GF180MCU/magic_designs/STI_parax.cir
.lib /usr/local/share/pdk/gf180mcuC/libs.tech/ngspice/sm141064.ngspice typical

Vdd VDD 0 3.3
Vbp BP VDD 2.7
Vbn BN GND -2.7
Vbias1 VB1 GND 1
Vbias15 VB15 GND 1.5
Vbias2 VB2 GND 0.5
Vin in 0 PWL(0 0 89.9n 0 90.1n 1.4 179.9n 1.4 180.1n 3.3 270n 3.3)
Vsw sw 0 PWL(0 0 250n 3.3)

.control
  save all
  tran 0.05n 250n
  write inv_tst2.raw
.endc


**** end user architecture code
**.ends
.end
